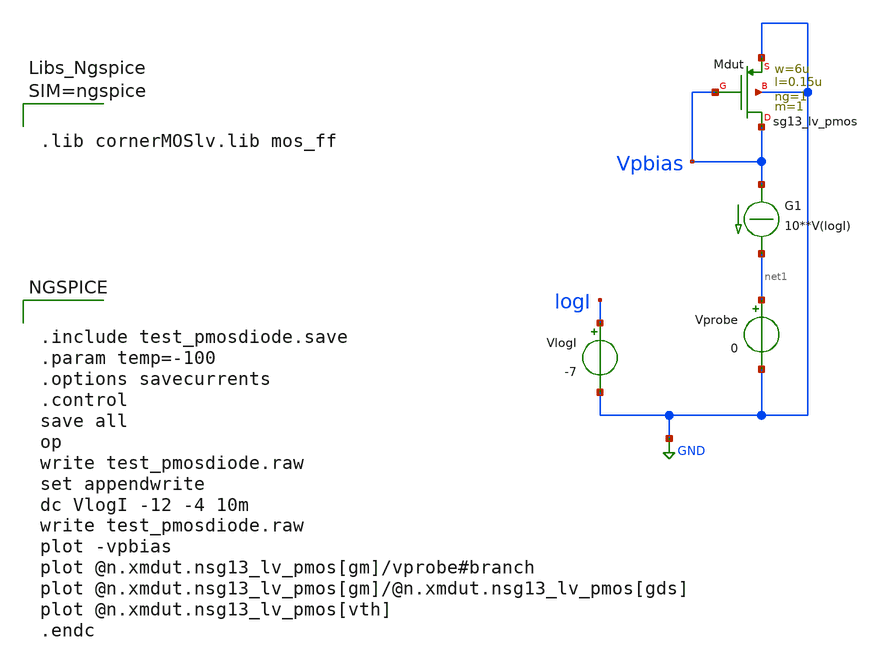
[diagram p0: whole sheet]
** sch_path: xschem/test_pmosdiode.sch
**.subckt test_pmosdiode
Vprobe net1 GND 0
.save i(vprobe)
G1 Vpbias net1 CUR=' 10**V(logI) '
VlogI logI GND -7
.save i(vlogi)
XMdut Vpbias Vpbias GND GND sg13_lv_pmos w=6u l=0.15u ng=1 m=1 mm_ok=1
**** begin user architecture code


.include test_pmosdiode.save
.param temp=-100
.options savecurrents
.control
save all
op
write test_pmosdiode.raw
set appendwrite
dc VlogI -12 -4 10m
write test_pmosdiode.raw
plot -vpbias
plot @n.xmdut.nsg13_lv_pmos[gm]/vprobe#branch
plot @n.xmdut.nsg13_lv_pmos[gm]/@n.xmdut.nsg13_lv_pmos[gds]
plot @n.xmdut.nsg13_lv_pmos[vth]
.endc





.lib cornerMOSlv.lib mos_ff



**** end user architecture code
**.ends
.GLOBAL GND
.end
